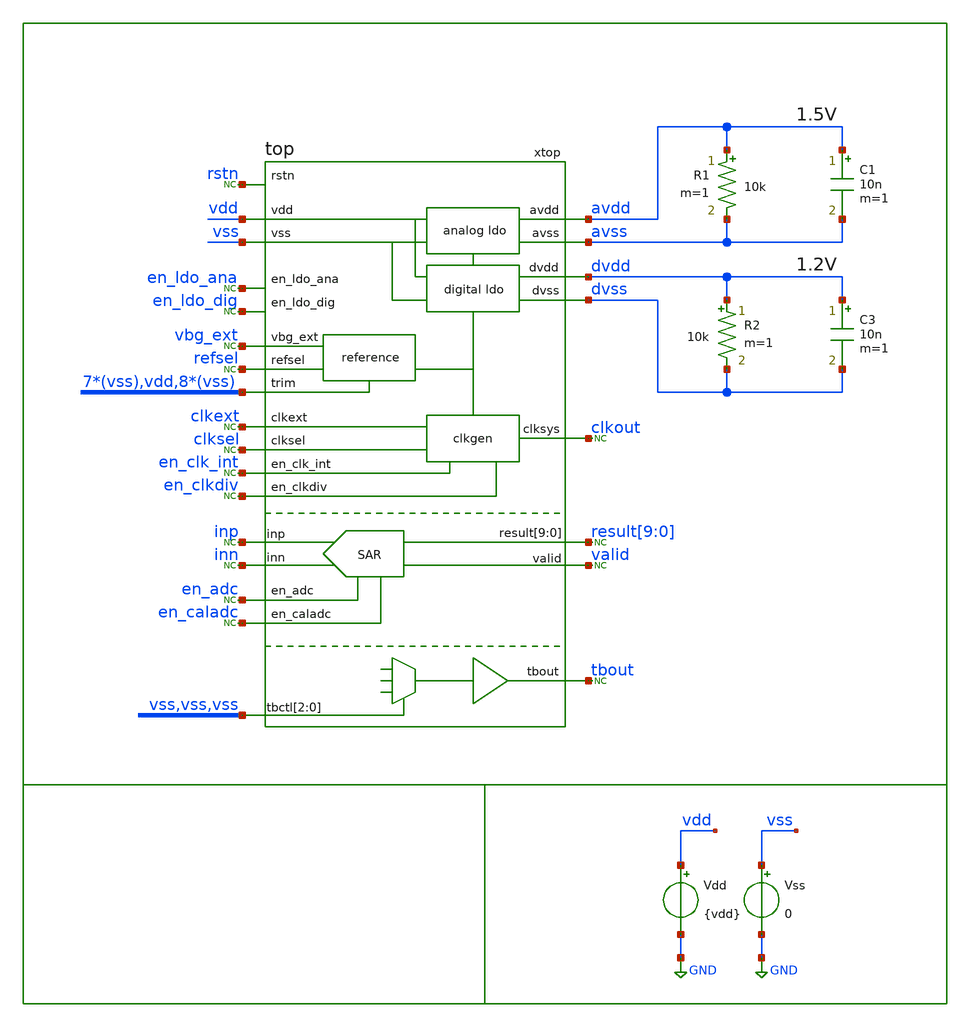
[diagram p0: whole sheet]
** sch_path: xschem/tb/top/tr_top.sch
**.subckt tr_top
C1 avdd avss 10n m=1
Vss vss GND 0
Vdd vdd GND {vdd}
* noconn valid
* noconn result[9:0]
R1 avdd avss 10k m=1
R2 dvdd dvss 10k m=1
xtop en_caladc dvdd inp result[9] result[8] result[7] result[6] result[5] result[4] result[3]
+ result[2] result[1] result[0] valid en_ldo_dig inn en_adc avdd rstn vdd vss en_ldo_ana clkout en_clk_int
+ clkext tbout en_clkdiv clksel refsel vbg_ext vss vss vss avss dvss vss vss vss vss vss vss vss vdd vss vss
+ vss vss vss vss vss vss top
* noconn tbout
* noconn rstn
* noconn clkext
* noconn vbg_ext
* noconn en_ldo_ana
* noconn en_ldo_dig
* noconn en_clk_int
* noconn en_clkdiv
* noconn en_adc
* noconn en_caladc
* noconn clksel
* noconn refsel
* noconn inp
* noconn inn
* noconn clkout
C3 dvdd dvss 10n m=1
**** begin user architecture code
* .include $::SKYWATER_STDCELLS/cells/
.include $::SKYWATER_STDCELLS/cells/buf/sky130_fd_sc_hd__buf_1.spice
.include $::SKYWATER_STDCELLS/cells/clkbuf/sky130_fd_sc_hd__clkbuf_1.spice
.include $::SKYWATER_STDCELLS/cells/clkbuf/sky130_fd_sc_hd__clkbuf_2.spice
.include $::SKYWATER_STDCELLS/cells/clkbuf/sky130_fd_sc_hd__clkbuf_4.spice
.include $::SKYWATER_STDCELLS/cells/clkbuf/sky130_fd_sc_hd__clkbuf_8.spice
.include $::SKYWATER_STDCELLS/cells/clkbuf/sky130_fd_sc_hd__clkbuf_16.spice
.include $::SKYWATER_STDCELLS/cells/decap/sky130_fd_sc_hd__decap_3.spice
.include $::SKYWATER_STDCELLS/cells/decap/sky130_fd_sc_hd__decap_4.spice
.include $::SKYWATER_STDCELLS/cells/decap/sky130_fd_sc_hd__decap_8.spice
.include $::SKYWATER_STDCELLS/cells/dfrbp/sky130_fd_sc_hd__dfrbp_1.spice
.include $::SKYWATER_STDCELLS/cells/dfrbp/sky130_fd_sc_hd__dfrbp_2.spice
.include $::SKYWATER_STDCELLS/cells/inv/sky130_fd_sc_hd__inv_1.spice
.include $::SKYWATER_STDCELLS/cells/inv/sky130_fd_sc_hd__inv_2.spice
.include $::SKYWATER_STDCELLS/cells/inv/sky130_fd_sc_hd__inv_4.spice
.include $::SKYWATER_STDCELLS/cells/mux2/sky130_fd_sc_hd__mux2_2.spice
.include $::SKYWATER_STDCELLS/cells/nand2/sky130_fd_sc_hd__nand2_1.spice
.include $::SKYWATER_STDCELLS/cells/tap/sky130_fd_sc_hd__tap_2.spice
.include $::SKYWATER_STDCELLS/cells/tapvpwrvgnd/sky130_fd_sc_hd__tapvpwrvgnd_1.spice

* Top-level Simulation setup

*-------------------------
* simulator setup
*-------------------------
.options method = gear
.options gmin   = 1e-12
.options abstol = 1e-10
.options chtol  = 1e-12
.options reltol = 100e-3
*-------------------------

*-------------------------
* simulator input
*-------------------------
.param MC_SWITCH=0
.param vdd=1.8

*-------------------------
* includes
*-------------------------
.include $::DESIGN_PATH/testbuffer/decoder3to8.spice

*-------------------------
* initial conditions
*-------------------------

.ic v(xtop.xsar.vp)=0
.ic v(xtop.xsar.vn)=0
.ic v(xtop.xsar.outp)=0
.ic v(xtop.xsar.outn)=0
.ic v(xtop.xsar.comp)=0

.ic v(xtop.xsar.ctlp_0_)=0
.ic v(xtop.xsar.ctlp_1_)=0
.ic v(xtop.xsar.ctlp_2_)=0
.ic v(xtop.xsar.ctlp_3_)=0
.ic v(xtop.xsar.ctlp_4_)=0
.ic v(xtop.xsar.ctlp_5_)=0
.ic v(xtop.xsar.ctlp_6_)=0
.ic v(xtop.xsar.ctlp_7_)=0
.ic v(xtop.xsar.ctlp_8_)=0
.ic v(xtop.xsar.ctlp_9_)=0

.ic v(xtop.xsar.ctln_0_)=0
.ic v(xtop.xsar.ctln_1_)=0
.ic v(xtop.xsar.ctln_2_)=0
.ic v(xtop.xsar.ctln_3_)=0
.ic v(xtop.xsar.ctln_4_)=0
.ic v(xtop.xsar.ctln_5_)=0
.ic v(xtop.xsar.ctln_6_)=0
.ic v(xtop.xsar.ctln_7_)=0
.ic v(xtop.xsar.ctln_8_)=0
.ic v(xtop.xsar.ctln_9_)=0

.ic v(xtop.xm.xbb.fb)=1.2

*-------------------------
* voltage sources
*-------------------------
vrstn rstn vss "pulse(1 0 100n 1n 1n 10u 200m)"
vclkext clkext vss 0
vbgext vbg_ext vss 1.2
ven_ldo_ana en_ldo_ana vss {vdd}
ven_ldo_dig en_ldo_dig vss {vdd}
ven_clk_int en_clk_int vss "pulse(0 1.8 105u 1n 1n 100m 200m)"
ven_clkdiv en_clkdiv vss 0
ven_adc en_adc vss "pulse(0 1.8 120u 1n 1n 100m 200m)"
vclksel clksel vss 0
vrefsel refsel vss {vdd}
vinp inp vss 0.75
vinn inn vss 0.75
vcaladc en_caladc vss 0

*-------------------------
* simulation
*-------------------------
*.tran 100e-9 120e-6 uic
.tran 100e-9 135e-6 uic
.control
save all
run
.endc
.end


* FET CORNERS
.include $::SKYWATER_MODELS/corners/tt.spice
*.include $::SKYWATER_MODELS/corners/ff.spice
*.include $::SKYWATER_MODELS/corners/ss.spice
*.include $::SKYWATER_MODELS/corners/sf.spice
*.include $::SKYWATER_MODELS/corners/fs.spice

* TT + R + C
*.include $::SKYWATER_MODELS/corners/tt_rmax_cmax.spice
*.include $::SKYWATER_MODELS/corners/tt_rmin_cmin.spice
*.include $::SKYWATER_MODELS/corners/tt_rmax_cmin.spice
*.include $::SKYWATER_MODELS/corners/tt_rmin_cmax.spice

* FF + R + C
*.include $::SKYWATER_MODELS/corners/ff_rmax_cmax.spice
*.include $::SKYWATER_MODELS/corners/ff_rmin_cmin.spice
*.include $::SKYWATER_MODELS/corners/ff_rmax_cmin.spice
*.include $::SKYWATER_MODELS/corners/ff_rmin_cmax.spice


* SS + R + C
*.include $::SKYWATER_MODELS/corners/ss_rmax_cmax.spice
*.include $::SKYWATER_MODELS/corners/ss_rmin_cmin.spice
*.include $::SKYWATER_MODELS/corners/ss_rmax_cmin.spice
*.include $::SKYWATER_MODELS/corners/ss_rmin_cmax.spice

* SF + R + C
*.include $::SKYWATER_MODELS/corners/sf_rmax_cmax.spice
*.include $::SKYWATER_MODELS/corners/sf_rmin_cmin.spice
*.include $::SKYWATER_MODELS/corners/sf_rmax_cmin.spice
*.include $::SKYWATER_MODELS/corners/sf_rmin_cmax.spice

* FS + R + C
*.include $::SKYWATER_MODELS/corners/fs_rmax_cmax.spice
*.include $::SKYWATER_MODELS/corners/fs_rmin_cmin.spice
*.include $::SKYWATER_MODELS/corners/fs_rmax_cmin.spice
*.include $::SKYWATER_MODELS/corners/fs_rmin_cmax.spice

**** end user architecture code
**.ends
.GLOBAL GND
.end
